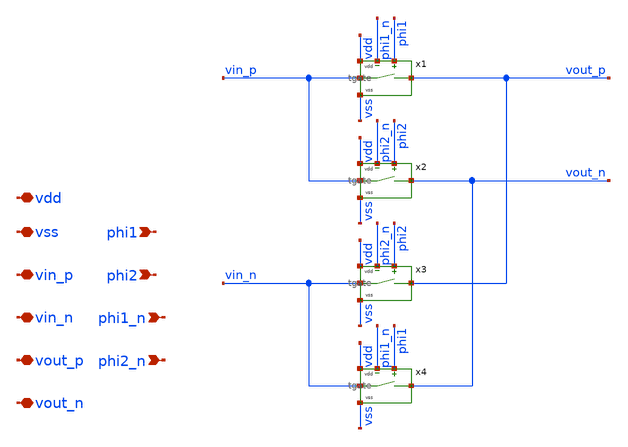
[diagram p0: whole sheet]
** sch_path: xschem/chopper/chopper.sch
**.subckt chopper vss vin_p vin_n vout_p vout_n phi1 phi2 phi1_n phi2_n vdd
*.iopin vss
*.iopin vin_p
*.iopin vin_n
*.iopin vout_p
*.iopin vout_n
*.ipin phi1
*.ipin phi2
*.ipin phi1_n
*.ipin phi2_n
*.iopin vdd
x1 vdd vin_p vss vout_p phi1_n phi1 tgate
x2 vdd vin_p vss vout_n phi2_n phi2 tgate
x3 vdd vin_n vss vout_p phi2_n phi2 tgate
x4 vdd vin_n vss vout_n phi1_n phi1 tgate
**.ends

* expanding   symbol:  tgate/tgate.sym # of pins=6
** sym_path: xschem/tgate/tgate.sym
** sch_path: xschem/tgate/tgate.sch
.subckt tgate vdd va vss vb en_n en
*.iopin vdd
*.iopin vss
*.iopin en
*.iopin va
*.iopin vb
*.iopin en_n
XM1 vb en va vss nfet_03v3 L=0.28u W=6.4u nf=4 ad='int((nf+1)/2) * W/nf * 0.18u' as='int((nf+2)/2) * W/nf * 0.18u'
+ pd='2*int((nf+1)/2) * (W/nf + 0.18u)' ps='2*int((nf+2)/2) * (W/nf + 0.18u)' nrd='0.18u / W' nrs='0.18u / W'
+ sa=0 sb=0 sd=0 m=1
XM2 va en_n vb vdd pfet_03v3 L=0.28u W=6.4u nf=4 ad='int((nf+1)/2) * W/nf * 0.18u' as='int((nf+2)/2) * W/nf * 0.18u'
+ pd='2*int((nf+1)/2) * (W/nf + 0.18u)' ps='2*int((nf+2)/2) * (W/nf + 0.18u)' nrd='0.18u / W' nrs='0.18u / W'
+ sa=0 sb=0 sd=0 m=1
.ends

.end
